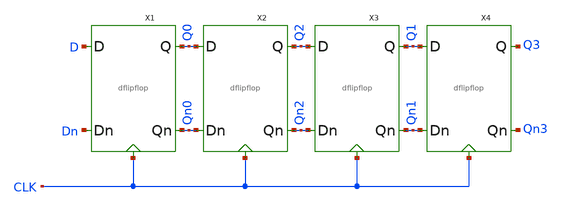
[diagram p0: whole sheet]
** sch_path: miniproject_02/xschem/shiftreg4.sch
**.subckt shiftreg4
X1 D Q0 Dn Qn0 CLK dflipflop
X2 Q0 Q2 Qn0 Qn2 CLK dflipflop
X3 Q2 Q1 Qn2 Qn1 CLK dflipflop
X4 Q1 Q3 Qn1 Qn3 CLK dflipflop
**.ends

* expanding   symbol:  ENGR3426-MADVLSI/miniproject_02/xschem/dflipflop.sym # of pins=5
** sym_path: miniproject_02/xschem/dflipflop.sym
** sch_path: miniproject_02/xschem/dflipflop.sch
.subckt dflipflop D Q Dn Qn CLK
*.ipin Dn
*.ipin D
*.opin Q
*.opin Qn
*.iopin CLK
XM1 net1 CLK D VDD sky130_fd_pr__pfet_01v8 L=0.15 W=1 nf=1 ad='int((nf+1)/2) * W/nf * 0.29' as='int((nf+2)/2) * W/nf * 0.29'
+ pd='2*int((nf+1)/2) * (W/nf + 0.29)' ps='2*int((nf+2)/2) * (W/nf + 0.29)' nrd='0.29 / W' nrs='0.29 / W'
+ sa=0 sb=0 sd=0 mult=1 m=1
XM2 net2 CLK Dn VDD sky130_fd_pr__pfet_01v8 L=0.15 W=1 nf=1 ad='int((nf+1)/2) * W/nf * 0.29' as='int((nf+2)/2) * W/nf * 0.29'
+ pd='2*int((nf+1)/2) * (W/nf + 0.29)' ps='2*int((nf+2)/2) * (W/nf + 0.29)' nrd='0.29 / W' nrs='0.29 / W'
+ sa=0 sb=0 sd=0 mult=1 m=1
XM3 Q CLK net1 GND sky130_fd_pr__nfet_01v8 L=0.15 W=1 nf=1 ad='int((nf+1)/2) * W/nf * 0.29' as='int((nf+2)/2) * W/nf * 0.29'
+ pd='2*int((nf+1)/2) * (W/nf + 0.29)' ps='2*int((nf+2)/2) * (W/nf + 0.29)' nrd='0.29 / W' nrs='0.29 / W'
+ sa=0 sb=0 sd=0 mult=1 m=1
XM4 Qn CLK net2 GND sky130_fd_pr__nfet_01v8 L=0.15 W=1 nf=1 ad='int((nf+1)/2) * W/nf * 0.29' as='int((nf+2)/2) * W/nf * 0.29'
+ pd='2*int((nf+1)/2) * (W/nf + 0.29)' ps='2*int((nf+2)/2) * (W/nf + 0.29)' nrd='0.29 / W' nrs='0.29 / W'
+ sa=0 sb=0 sd=0 mult=1 m=1
XM5 net4 CLK GND GND sky130_fd_pr__nfet_01v8 L=0.15 W=4 nf=1 ad='int((nf+1)/2) * W/nf * 0.29' as='int((nf+2)/2) * W/nf * 0.29'
+ pd='2*int((nf+1)/2) * (W/nf + 0.29)' ps='2*int((nf+2)/2) * (W/nf + 0.29)' nrd='0.29 / W' nrs='0.29 / W'
+ sa=0 sb=0 sd=0 mult=1 m=1
XM6 net2 net1 net4 GND sky130_fd_pr__nfet_01v8 L=0.15 W=1 nf=1 ad='int((nf+1)/2) * W/nf * 0.29' as='int((nf+2)/2) * W/nf * 0.29'
+ pd='2*int((nf+1)/2) * (W/nf + 0.29)' ps='2*int((nf+2)/2) * (W/nf + 0.29)' nrd='0.29 / W' nrs='0.29 / W'
+ sa=0 sb=0 sd=0 mult=1 m=1
XM7 net4 net2 net1 GND sky130_fd_pr__nfet_01v8 L=0.15 W=1 nf=1 ad='int((nf+1)/2) * W/nf * 0.29' as='int((nf+2)/2) * W/nf * 0.29'
+ pd='2*int((nf+1)/2) * (W/nf + 0.29)' ps='2*int((nf+2)/2) * (W/nf + 0.29)' nrd='0.29 / W' nrs='0.29 / W'
+ sa=0 sb=0 sd=0 mult=1 m=1
XM8 net2 net1 VDD VDD sky130_fd_pr__pfet_01v8 L=0.15 W=1 nf=1 ad='int((nf+1)/2) * W/nf * 0.29' as='int((nf+2)/2) * W/nf * 0.29'
+ pd='2*int((nf+1)/2) * (W/nf + 0.29)' ps='2*int((nf+2)/2) * (W/nf + 0.29)' nrd='0.29 / W' nrs='0.29 / W'
+ sa=0 sb=0 sd=0 mult=1 m=1
XM9 VDD net2 net1 VDD sky130_fd_pr__pfet_01v8 L=0.15 W=1 nf=1 ad='int((nf+1)/2) * W/nf * 0.29' as='int((nf+2)/2) * W/nf * 0.29'
+ pd='2*int((nf+1)/2) * (W/nf + 0.29)' ps='2*int((nf+2)/2) * (W/nf + 0.29)' nrd='0.29 / W' nrs='0.29 / W'
+ sa=0 sb=0 sd=0 mult=1 m=1
XM10 net3 CLK VDD VDD sky130_fd_pr__pfet_01v8 L=0.15 W=4 nf=1 ad='int((nf+1)/2) * W/nf * 0.29' as='int((nf+2)/2) * W/nf * 0.29'
+ pd='2*int((nf+1)/2) * (W/nf + 0.29)' ps='2*int((nf+2)/2) * (W/nf + 0.29)' nrd='0.29 / W' nrs='0.29 / W'
+ sa=0 sb=0 sd=0 mult=1 m=1
XM11 Qn Q net3 VDD sky130_fd_pr__pfet_01v8 L=0.15 W=1 nf=1 ad='int((nf+1)/2) * W/nf * 0.29' as='int((nf+2)/2) * W/nf * 0.29'
+ pd='2*int((nf+1)/2) * (W/nf + 0.29)' ps='2*int((nf+2)/2) * (W/nf + 0.29)' nrd='0.29 / W' nrs='0.29 / W'
+ sa=0 sb=0 sd=0 mult=1 m=1
XM12 net3 Qn Q VDD sky130_fd_pr__pfet_01v8 L=0.15 W=1 nf=1 ad='int((nf+1)/2) * W/nf * 0.29' as='int((nf+2)/2) * W/nf * 0.29'
+ pd='2*int((nf+1)/2) * (W/nf + 0.29)' ps='2*int((nf+2)/2) * (W/nf + 0.29)' nrd='0.29 / W' nrs='0.29 / W'
+ sa=0 sb=0 sd=0 mult=1 m=1
XM13 Qn Q GND GND sky130_fd_pr__nfet_01v8 L=0.15 W=1 nf=1 ad='int((nf+1)/2) * W/nf * 0.29' as='int((nf+2)/2) * W/nf * 0.29'
+ pd='2*int((nf+1)/2) * (W/nf + 0.29)' ps='2*int((nf+2)/2) * (W/nf + 0.29)' nrd='0.29 / W' nrs='0.29 / W'
+ sa=0 sb=0 sd=0 mult=1 m=1
XM14 GND Qn Q GND sky130_fd_pr__nfet_01v8 L=0.15 W=1 nf=1 ad='int((nf+1)/2) * W/nf * 0.29' as='int((nf+2)/2) * W/nf * 0.29'
+ pd='2*int((nf+1)/2) * (W/nf + 0.29)' ps='2*int((nf+2)/2) * (W/nf + 0.29)' nrd='0.29 / W' nrs='0.29 / W'
+ sa=0 sb=0 sd=0 mult=1 m=1
.ends

.GLOBAL VDD
.GLOBAL GND
.end
